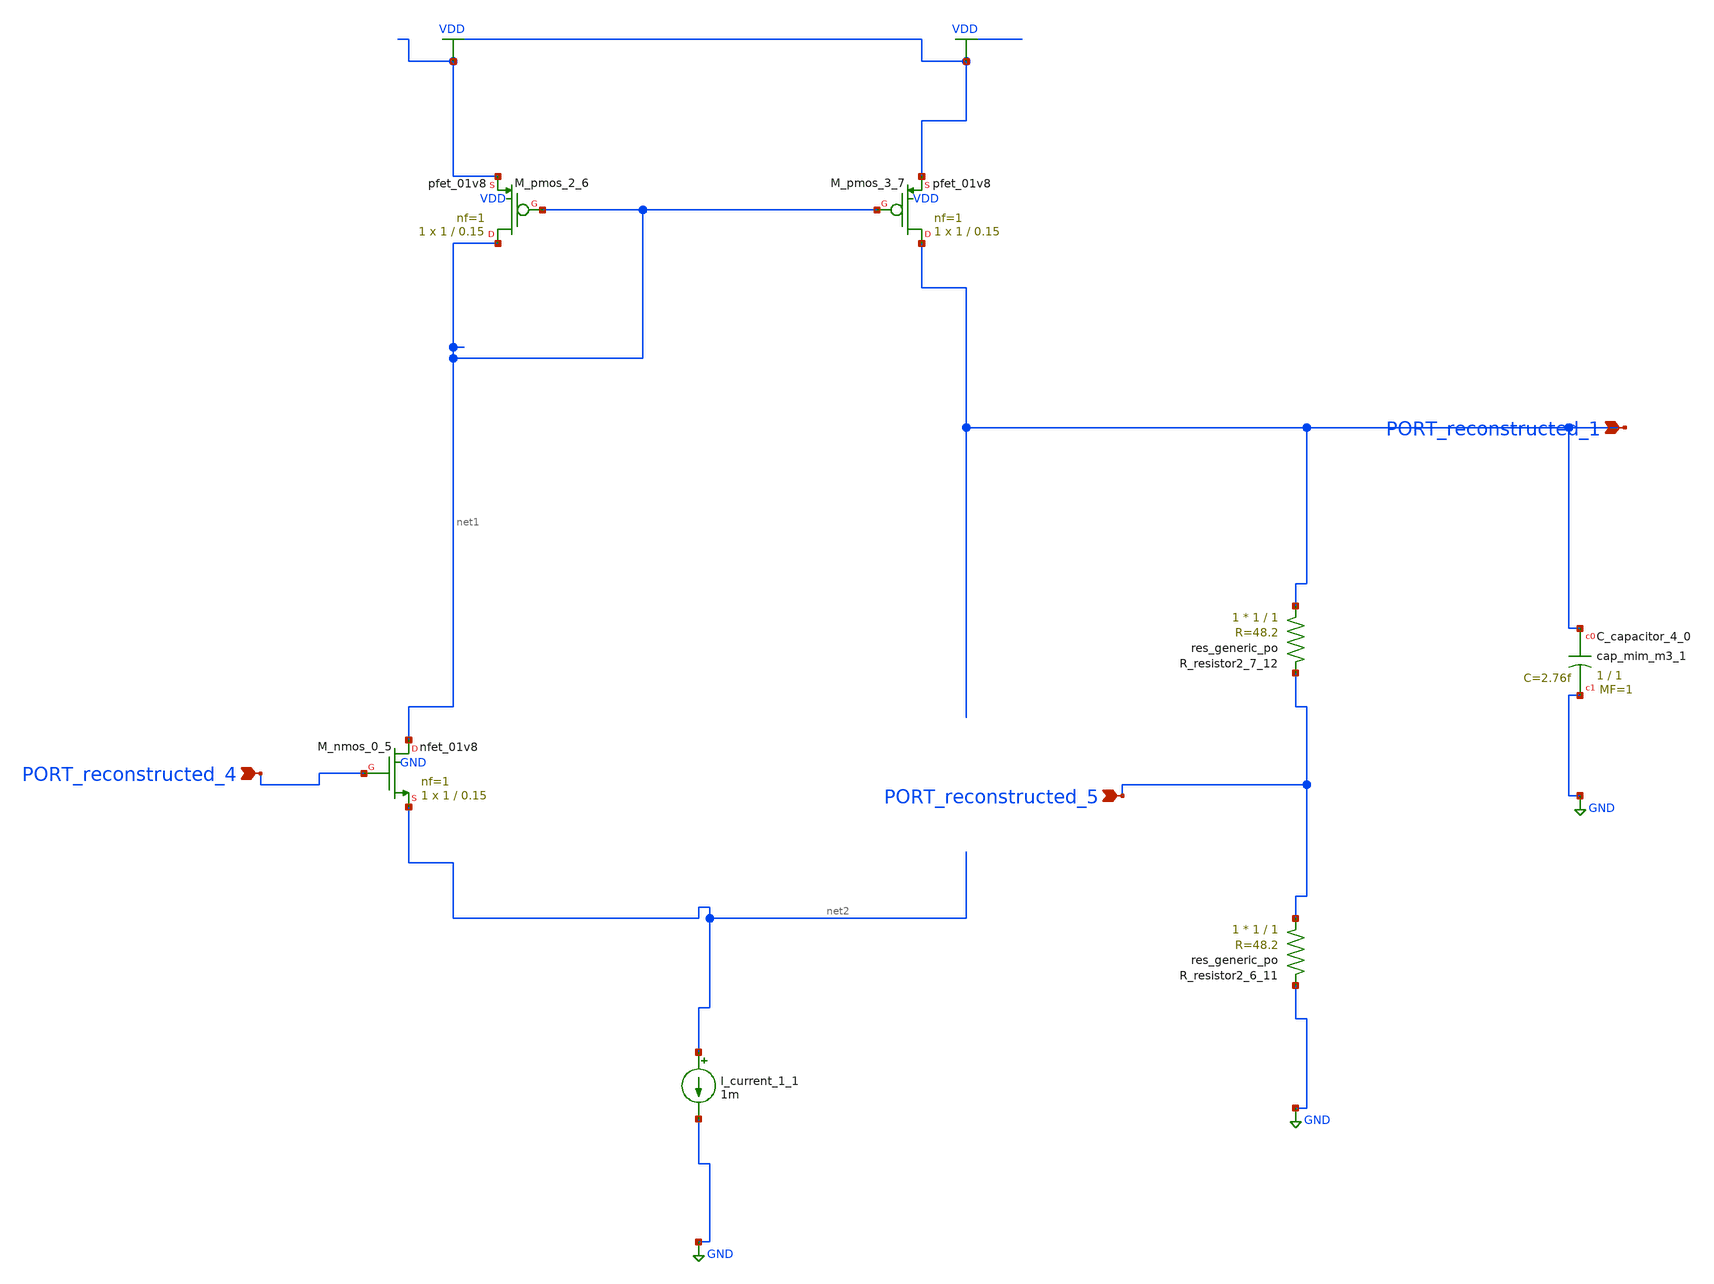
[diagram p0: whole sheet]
** sch_path: schematics/AMSNet/687.sch
**.subckt 687 PORT_reconstructed_1 PORT_reconstructed_4 PORT_reconstructed_5
*.ipin PORT_reconstructed_1
*.ipin PORT_reconstructed_4
*.ipin PORT_reconstructed_5
XC_capacitor_4_0 PORT_reconstructed_1 GND sky130_fd_pr__cap_mim_m3_1 W=1 L=1 MF=1 m=1
I_current_1_1 net2 GND 1m
XM_nmos_0_5 net1 PORT_reconstructed_4 net2 GND sky130_fd_pr__nfet_01v8 L=0.15 W=1 nf=1 ad='int((1 + 1)/2) * 1 / 1 * 0.29'
+ as='int((1 + 2)/2) * 1 / 1 * 0.29' pd='2*int((1 + 1)/2) * (1 / 1 + 0.29)' ps='2*int((1 + 2)/2) * (1 / 1 + 0.29)'
+ nrd='0.29 / 1 ' nrs='0.29 / 1 ' sa=0 sb=0 sd=0 mult=1 m=1
XM_pmos_2_6 net1 net1 VDD VDD sky130_fd_pr__pfet_01v8 L=0.15 W=1 nf=1 ad='int((1 + 1)/2) * 1 / 1 * 0.29'
+ as='int((1 + 2)/2) * 1 / 1 * 0.29' pd='2*int((1 + 1)/2) * (1 / 1 + 0.29)' ps='2*int((1 + 2)/2) * (1 / 1 + 0.29)'
+ nrd='0.29 / 1 ' nrs='0.29 / 1 ' sa=0 sb=0 sd=0 mult=1 m=1
XM_pmos_3_7 PORT_reconstructed_1 net1 VDD VDD sky130_fd_pr__pfet_01v8 L=0.15 W=1 nf=1 ad='int((1 + 1)/2) * 1 / 1 * 0.29'
+ as='int((1 + 2)/2) * 1 / 1 * 0.29' pd='2*int((1 + 1)/2) * (1 / 1 + 0.29)' ps='2*int((1 + 2)/2) * (1 / 1 + 0.29)'
+ nrd='0.29 / 1 ' nrs='0.29 / 1 ' sa=0 sb=0 sd=0 mult=1 m=1
XR_resistor2_6_11 PORT_reconstructed_5 GND sky130_fd_pr__res_generic_po W=1 L=1 m=1
XR_resistor2_7_12 PORT_reconstructed_1 PORT_reconstructed_5 sky130_fd_pr__res_generic_po W=1 L=1 m=1
**.ends
.GLOBAL GND
.GLOBAL VDD
.end
